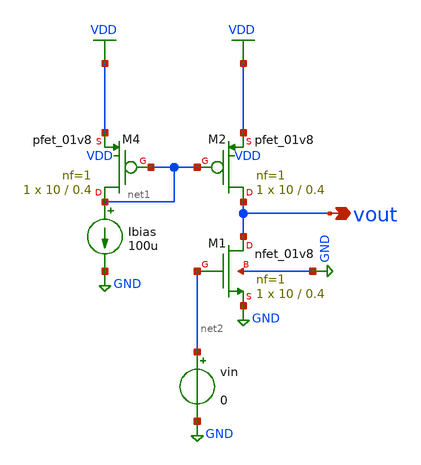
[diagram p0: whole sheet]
** sch_path: SelfStudy/Analog/Tony Chan/SpiceSim/cs.sch
**.subckt cs vout
*.opin vout
XM1 vout net2 GND GND sky130_fd_pr__nfet_01v8 L=0.4 W=10 nf=1 ad='int((1 + 1)/2) * 10 / 1 * 0.29' as='int((1 + 2)/2) * 10 / 1 * 0.29'
+ pd='2*int((1 + 1)/2) * (10 / 1 + 0.29)' ps='2*int((1 + 2)/2) * (10 / 1 + 0.29)' nrd='0.29 / 10 ' nrs='0.29 / 10 '
+ sa=0 sb=0 sd=0 mult=1 m=1
Ibias net1 GND 100u
XM2 vout net1 VDD VDD sky130_fd_pr__pfet_01v8 L=0.4 W=10 nf=1 ad='int((1 + 1)/2) * 10 / 1 * 0.29' as='int((1 + 2)/2) * 10 / 1 * 0.29'
+ pd='2*int((1 + 1)/2) * (10 / 1 + 0.29)' ps='2*int((1 + 2)/2) * (10 / 1 + 0.29)' nrd='0.29 / 10 ' nrs='0.29 / 10 '
+ sa=0 sb=0 sd=0 mult=1 m=1
XM4 net1 net1 VDD VDD sky130_fd_pr__pfet_01v8 L=0.4 W=10 nf=1 ad='int((1 + 1)/2) * 10 / 1 * 0.29' as='int((1 + 2)/2) * 10 / 1 * 0.29'
+ pd='2*int((1 + 1)/2) * (10 / 1 + 0.29)' ps='2*int((1 + 2)/2) * (10 / 1 + 0.29)' nrd='0.29 / 10 ' nrs='0.29 / 10 '
+ sa=0 sb=0 sd=0 mult=1 m=1
vin net2 GND 0
**** begin user architecture code

.lib /usr/local/share/pdk/sky130A/libs.tech/ngspice/sky130.lib.spice tt
vsup VDD 0 1.8
.end
.control
op
dc vin 0 1.8 0.01
set plot gain
write gain.raw
.endc


**** end user architecture code
**.ends
.GLOBAL GND
.GLOBAL VDD
.end
